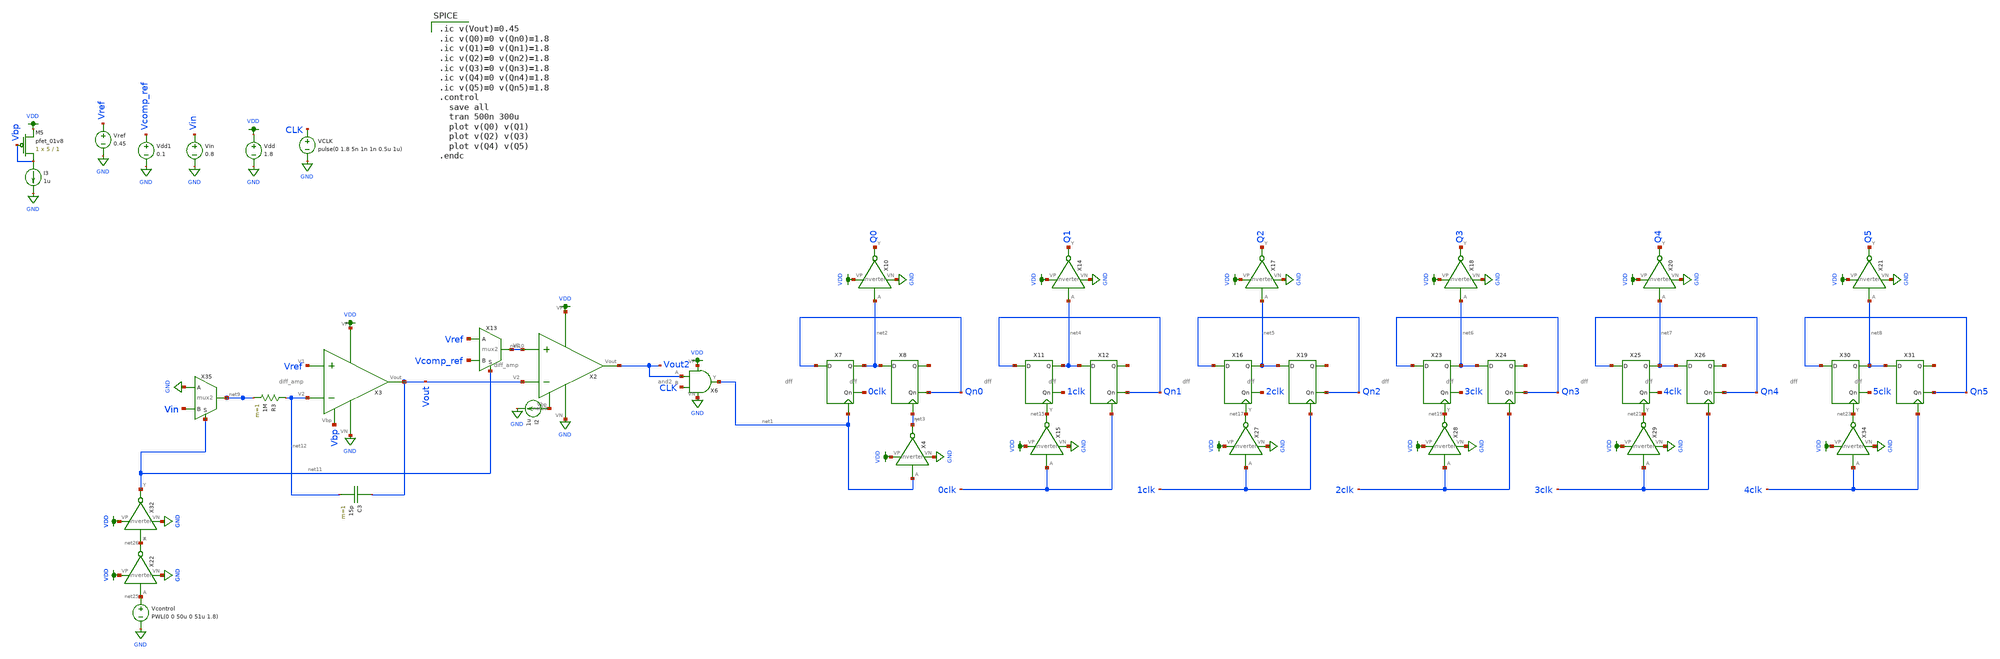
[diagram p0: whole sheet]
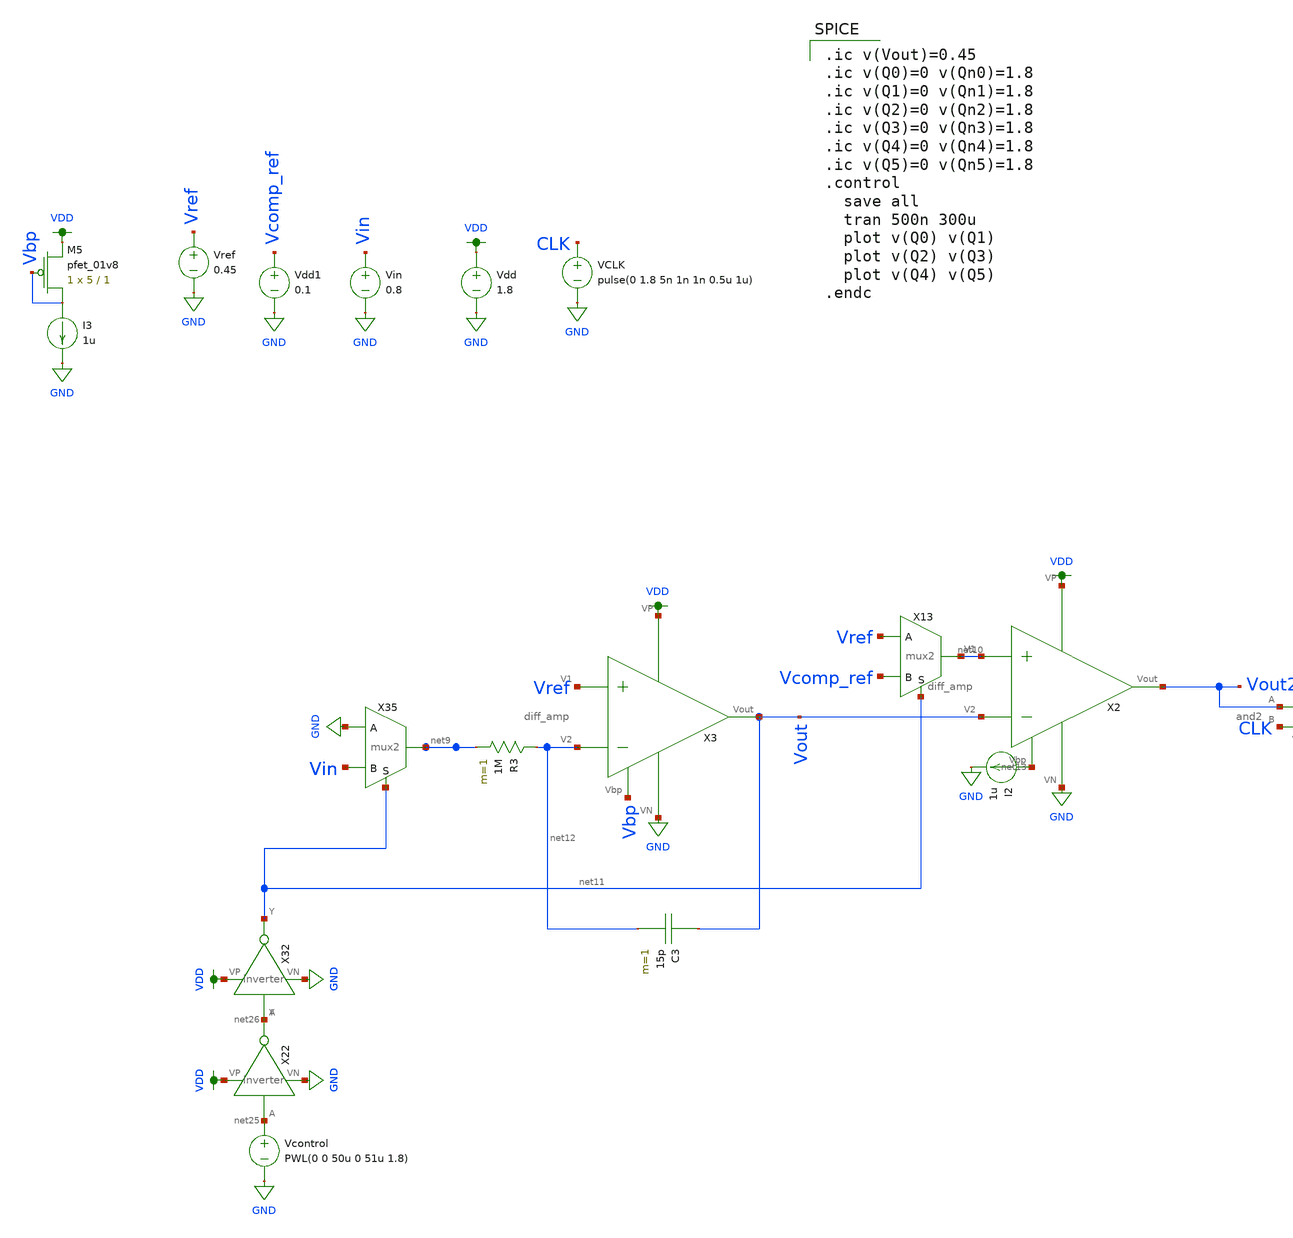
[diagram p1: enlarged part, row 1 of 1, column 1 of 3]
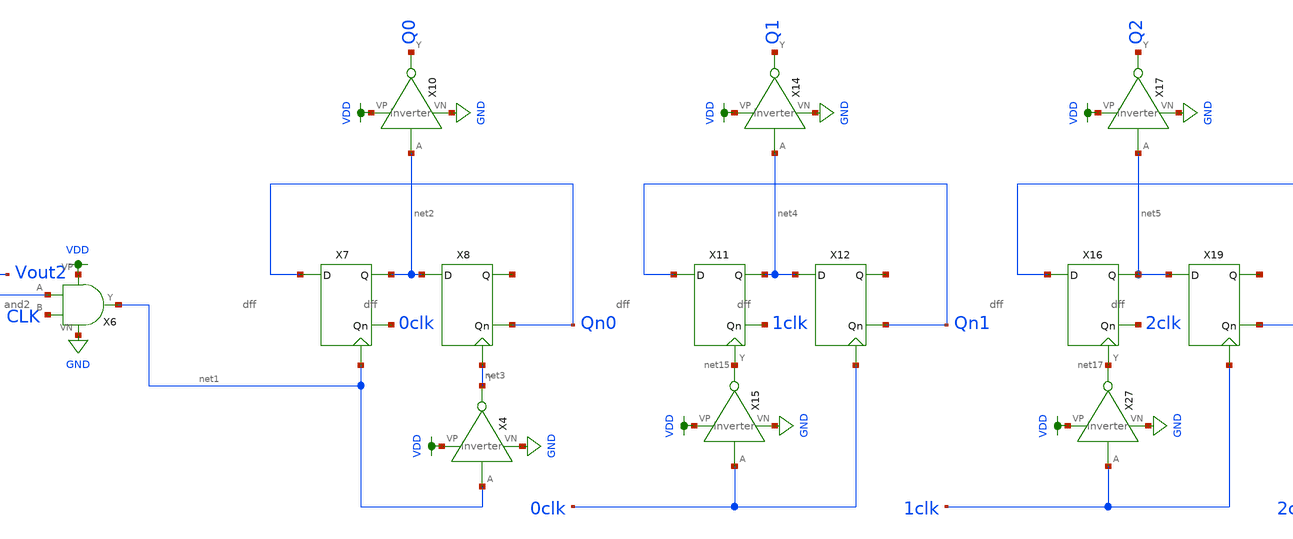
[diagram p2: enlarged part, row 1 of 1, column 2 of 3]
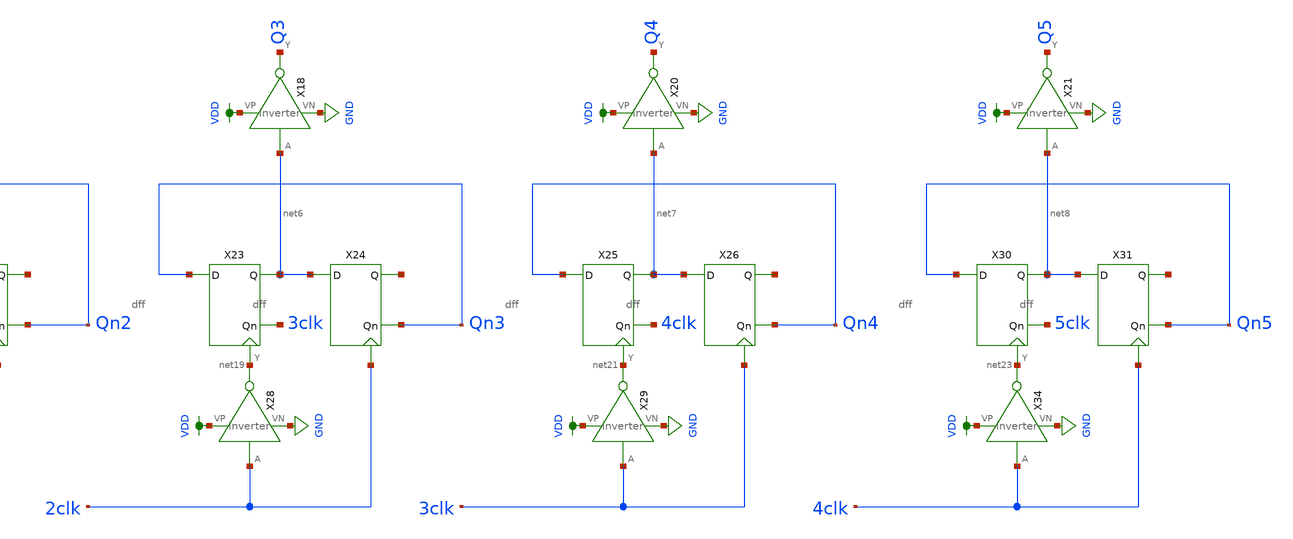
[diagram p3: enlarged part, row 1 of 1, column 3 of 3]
** sch_path: schematic/double-slope-works.sch
**.subckt double-slope-works
X2 VDD net13 Vout2 net10 Vout GND diff_amp
Vdd VDD GND 1.8
VCLK CLK GND pulse(0 1.8 5n 1n 1n 0.5u 1u)
Vdd1 Vcomp_ref GND 0.1
Vin Vin GND 0.8
I2 net13 GND 1u
X6 VDD Vout2 GND net1 CLK and2
X7 Qn0 0clk net2 net1 dff
X8 net2 Qn0 net14 net3 dff
X10 net2 Q0 VDD GND inverter
X11 Qn1 1clk net4 net15 dff
X12 net4 Qn1 net16 0clk dff
X15 0clk net15 VDD GND inverter
X16 Qn2 2clk net5 net17 dff
X19 net5 Qn2 net18 1clk dff
X23 Qn3 3clk net6 net19 dff
X24 net6 Qn3 net20 2clk dff
X25 Qn4 4clk net7 net21 dff
X26 net7 Qn4 net22 3clk dff
X27 1clk net17 VDD GND inverter
X28 2clk net19 VDD GND inverter
X29 3clk net21 VDD GND inverter
X30 Qn5 5clk net8 net23 dff
X31 net8 Qn5 net24 4clk dff
X34 4clk net23 VDD GND inverter
X13 net10 Vref Vcomp_ref net11 mux2
Vcontrol net25 GND PWL(0 0 50u 0 51u 1.8)
X14 net4 Q1 VDD GND inverter
X17 net5 Q2 VDD GND inverter
X18 net6 Q3 VDD GND inverter
X20 net7 Q4 VDD GND inverter
X21 net8 Q5 VDD GND inverter
X22 net25 net26 VDD GND inverter
X32 net26 net11 VDD GND inverter
X35 net9 GND Vin net11 mux2
X4 net1 net3 VDD GND inverter
XM5 Vbp Vbp VDD VDD sky130_fd_pr__pfet_01v8 L=1 W=5 nf=1 ad='int((nf+1)/2) * W/nf * 0.29' as='int((nf+2)/2) * W/nf * 0.29'
+ pd='2*int((nf+1)/2) * (W/nf + 0.29)' ps='2*int((nf+2)/2) * (W/nf + 0.29)' nrd='0.29 / W' nrs='0.29 / W'
+ sa=0 sb=0 sd=0 mult=1 m=1
I3 Vbp GND 1u
C3 Vout net12 15p m=1
X3 VDD Vbp Vout Vref net12 GND diff_amp
R3 net12 net9 1M m=1
Vref Vref GND 0.45
**** begin user architecture code

.ic v(Vout)=0.45
.ic v(Q0)=0 v(Qn0)=1.8
.ic v(Q1)=0 v(Qn1)=1.8
.ic v(Q2)=0 v(Qn2)=1.8
.ic v(Q3)=0 v(Qn3)=1.8
.ic v(Q4)=0 v(Qn4)=1.8
.ic v(Q5)=0 v(Qn5)=1.8
.control
  save all
  tran 500n 300u
  plot v(Q0) v(Q1)
  plot v(Q2) v(Q3)
  plot v(Q4) v(Q5)
.endc


.option wnflag=1
.param MC_SWITCH=0.0
.lib ~/skywater/skywater-pdk/libraries/sky130_fd_pr_ngspice/latest/models/sky130.lib.spice tt

**** end user architecture code
**.ends
.GLOBAL GND
.GLOBAL VDD
.end
